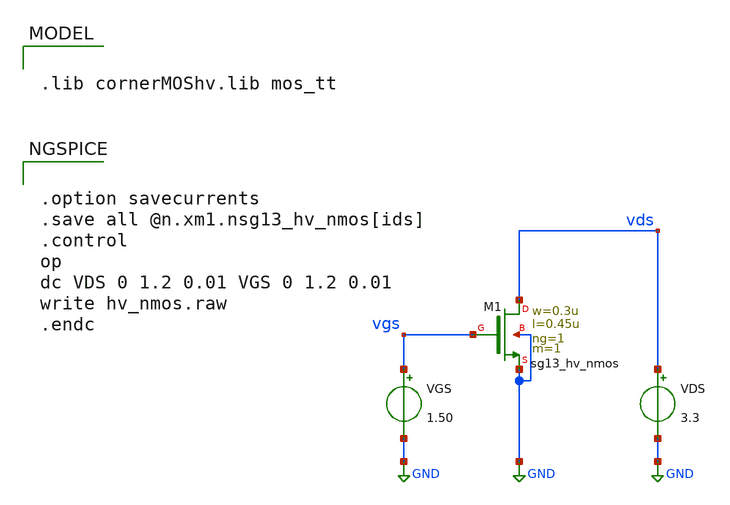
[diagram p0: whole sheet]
** sch_path: gmid/hv_nmos.sch
**.subckt hv_nmos
XM1 vds vgs GND GND sg13_hv_nmos w=0.3u l=0.45u ng=1 m=1 mm_ok=1
VGS vgs GND 1.50
VDS vds GND 3.3
**** begin user architecture code

.lib cornerMOShv.lib mos_tt



.option savecurrents
.save all @n.xm1.nsg13_hv_nmos[ids]
.control
op
dc VDS 0 1.2 0.01 VGS 0 1.2 0.01
write hv_nmos.raw
.endc


**** end user architecture code
**.ends
.GLOBAL GND
.end
